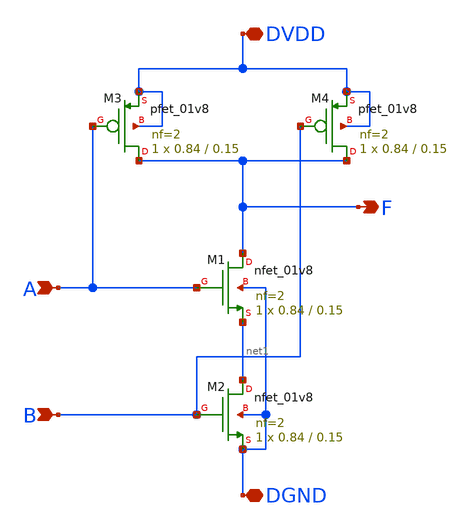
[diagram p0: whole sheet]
** sch_path: mywork/nand2x1/cell/nand2x1.sch
**.subckt nand2x1 DVDD DGND A B F
*.iopin DVDD
*.iopin DGND
*.ipin A
*.ipin B
*.opin F
XM1 F A net1 DGND sky130_fd_pr__nfet_01v8 L=0.15 W=0.84 nf=2 ad='int((nf+1)/2) * W/nf * 0.29' as='int((nf+2)/2) * W/nf * 0.29'
+ pd='2*int((nf+1)/2) * (W/nf + 0.29)' ps='2*int((nf+2)/2) * (W/nf + 0.29)' nrd='0.29 / W' nrs='0.29 / W'
+ sa=0 sb=0 sd=0 mult=1 m=1
XM2 net1 B DGND DGND sky130_fd_pr__nfet_01v8 L=0.15 W=0.84 nf=2 ad='int((nf+1)/2) * W/nf * 0.29' as='int((nf+2)/2) * W/nf * 0.29'
+ pd='2*int((nf+1)/2) * (W/nf + 0.29)' ps='2*int((nf+2)/2) * (W/nf + 0.29)' nrd='0.29 / W' nrs='0.29 / W'
+ sa=0 sb=0 sd=0 mult=1 m=1
XM3 F A DVDD DVDD sky130_fd_pr__pfet_01v8 L=0.15 W=0.84 nf=2 ad='int((nf+1)/2) * W/nf * 0.29' as='int((nf+2)/2) * W/nf * 0.29'
+ pd='2*int((nf+1)/2) * (W/nf + 0.29)' ps='2*int((nf+2)/2) * (W/nf + 0.29)' nrd='0.29 / W' nrs='0.29 / W'
+ sa=0 sb=0 sd=0 mult=1 m=1
XM4 F B DVDD DVDD sky130_fd_pr__pfet_01v8 L=0.15 W=0.84 nf=2 ad='int((nf+1)/2) * W/nf * 0.29' as='int((nf+2)/2) * W/nf * 0.29'
+ pd='2*int((nf+1)/2) * (W/nf + 0.29)' ps='2*int((nf+2)/2) * (W/nf + 0.29)' nrd='0.29 / W' nrs='0.29 / W'
+ sa=0 sb=0 sd=0 mult=1 m=1
**.ends
.end
